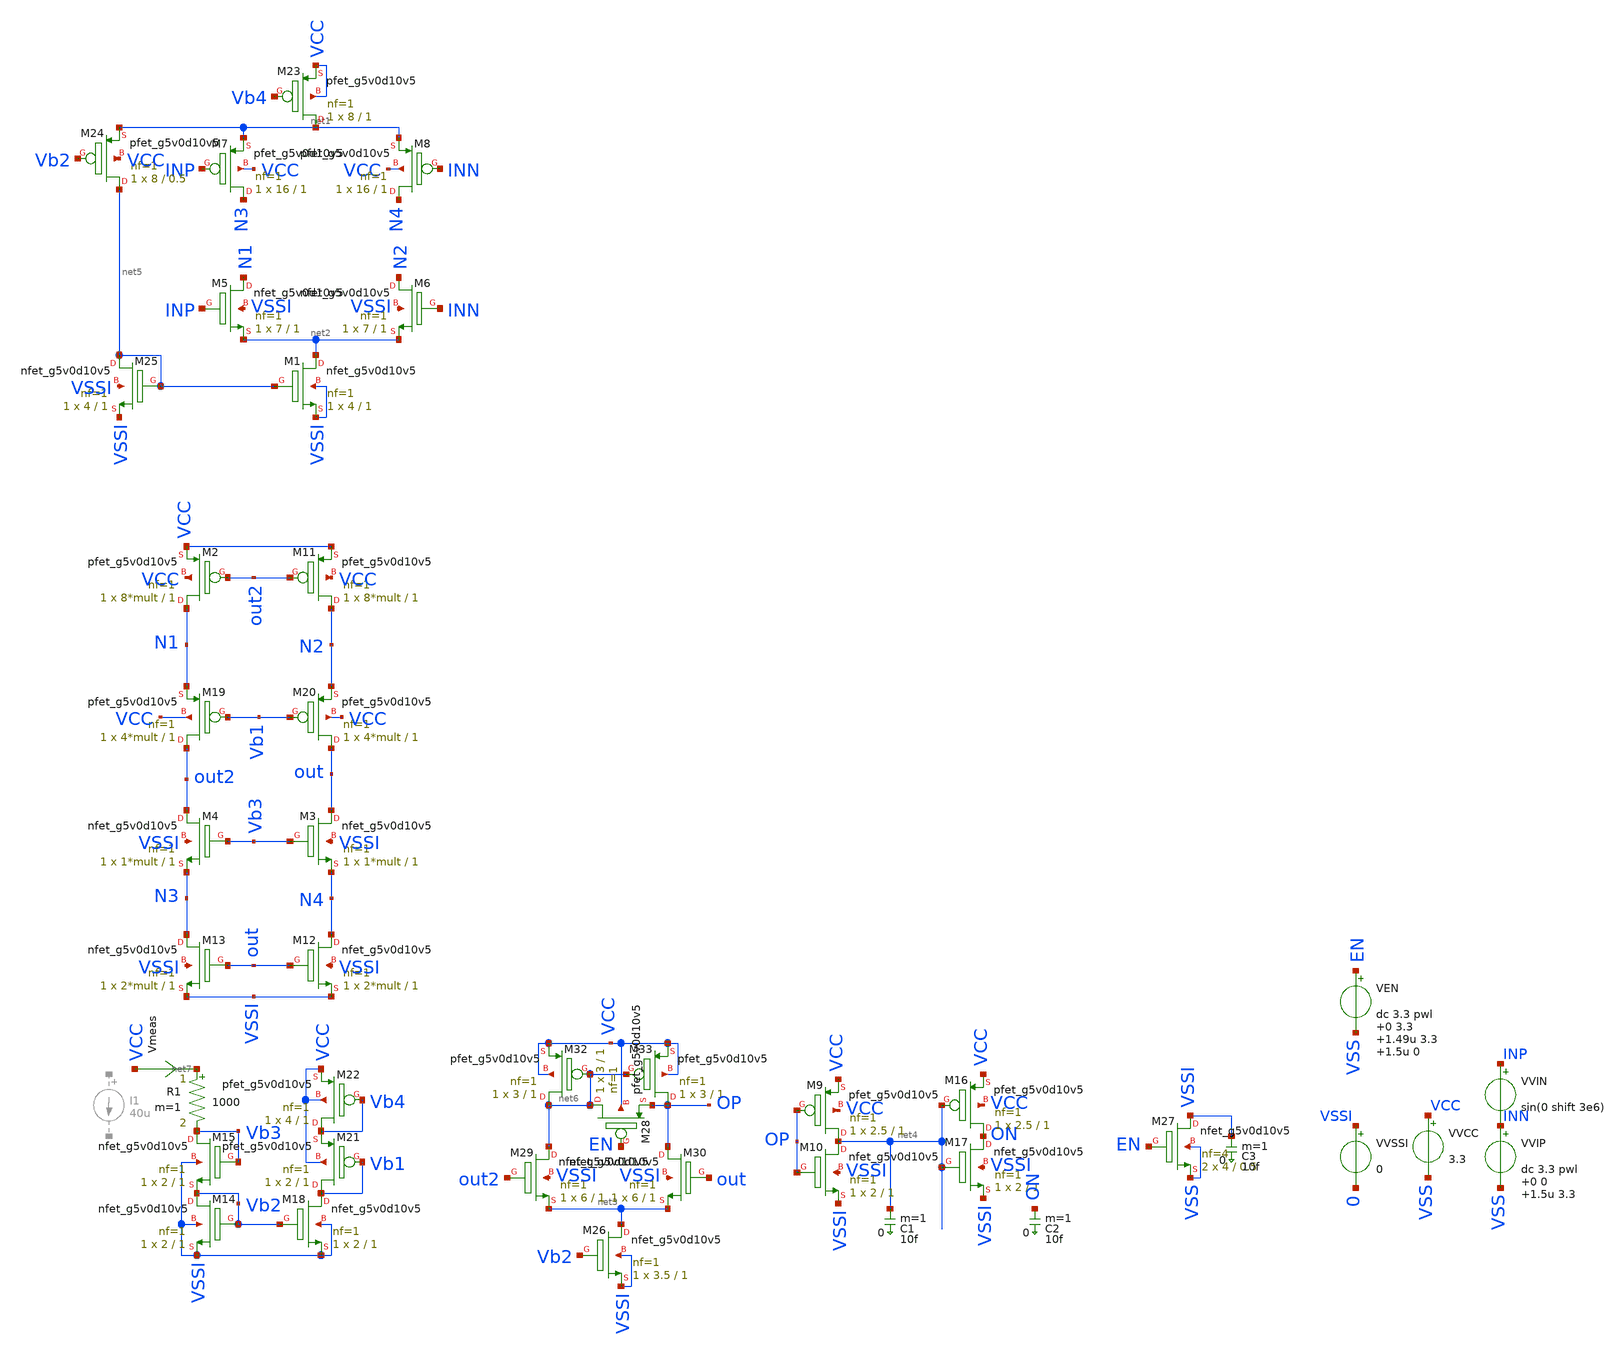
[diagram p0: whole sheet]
** sch_path: folded_cascode/folded_cascode.sch
.lib $::SKYWATER_MODELS/sky130.lib.spice.ss.red ss
.include $::SKYWATER_STDCELLS/sky130_fd_sc_hd.spice

**.subckt folded_cascode
VVIN INP INN sin(0 shift 3e6)
VVSSI VSSI 0 0
VVCC VCC VSS 3.3
XM19 out2 Vb1 N1 VCC sky130_fd_pr__pfet_g5v0d10v5 L=1 W=4*mult nf=1 ad='int((nf+1)/2) * W/nf * 0.29'
+ as='int((nf+2)/2) * W/nf * 0.29' pd='2*int((nf+1)/2) * (W/nf + 0.29)' ps='2*int((nf+2)/2) * (W/nf + 0.29)'
+ nrd='0.29 / W' nrs='0.29 / W' sa=0 sb=0 sd=0 mult=1 m=1
XM20 out Vb1 N2 VCC sky130_fd_pr__pfet_g5v0d10v5 L=1 W=4*mult nf=1 ad='int((nf+1)/2) * W/nf * 0.29' as='int((nf+2)/2) * W/nf * 0.29'
+ pd='2*int((nf+1)/2) * (W/nf + 0.29)' ps='2*int((nf+2)/2) * (W/nf + 0.29)' nrd='0.29 / W' nrs='0.29 / W'
+ sa=0 sb=0 sd=0 mult=1 m=1
XM3 out Vb3 N4 VSSI sky130_fd_pr__nfet_g5v0d10v5 L=1 W=1*mult nf=1 ad='int((nf+1)/2) * W/nf * 0.29' as='int((nf+2)/2) * W/nf * 0.29'
+ pd='2*int((nf+1)/2) * (W/nf + 0.29)' ps='2*int((nf+2)/2) * (W/nf + 0.29)' nrd='0.29 / W' nrs='0.29 / W'
+ sa=0 sb=0 sd=0 mult=1 m=1
XM4 out2 Vb3 N3 VSSI sky130_fd_pr__nfet_g5v0d10v5 L=1 W=1*mult nf=1 ad='int((nf+1)/2) * W/nf * 0.29'
+ as='int((nf+2)/2) * W/nf * 0.29' pd='2*int((nf+1)/2) * (W/nf + 0.29)' ps='2*int((nf+2)/2) * (W/nf + 0.29)'
+ nrd='0.29 / W' nrs='0.29 / W' sa=0 sb=0 sd=0 mult=1 m=1
VVIP INN VSS dc 3.3 pwl 0 0 1.5u 3.3

XM5 N1 INP net2 VSSI sky130_fd_pr__nfet_g5v0d10v5 L=1 W=7 nf=1 ad='int((nf+1)/2) * W/nf * 0.29' as='int((nf+2)/2) * W/nf * 0.29'
+ pd='2*int((nf+1)/2) * (W/nf + 0.29)' ps='2*int((nf+2)/2) * (W/nf + 0.29)' nrd='0.29 / W' nrs='0.29 / W'
+ sa=0 sb=0 sd=0 mult=1 m=1
XM6 N2 INN net2 VSSI sky130_fd_pr__nfet_g5v0d10v5 L=1 W=7 nf=1 ad='int((nf+1)/2) * W/nf * 0.29' as='int((nf+2)/2) * W/nf * 0.29'
+ pd='2*int((nf+1)/2) * (W/nf + 0.29)' ps='2*int((nf+2)/2) * (W/nf + 0.29)' nrd='0.29 / W' nrs='0.29 / W'
+ sa=0 sb=0 sd=0 mult=1 m=1
XM7 N3 INP net1 VCC sky130_fd_pr__pfet_g5v0d10v5 L=1 W=16 nf=1 ad='int((nf+1)/2) * W/nf * 0.29' as='int((nf+2)/2) * W/nf * 0.29'
+ pd='2*int((nf+1)/2) * (W/nf + 0.29)' ps='2*int((nf+2)/2) * (W/nf + 0.29)' nrd='0.29 / W' nrs='0.29 / W'
+ sa=0 sb=0 sd=0 mult=1 m=1
XM8 N4 INN net1 VCC sky130_fd_pr__pfet_g5v0d10v5 L=1 W=16 nf=1 ad='int((nf+1)/2) * W/nf * 0.29' as='int((nf+2)/2) * W/nf * 0.29'
+ pd='2*int((nf+1)/2) * (W/nf + 0.29)' ps='2*int((nf+2)/2) * (W/nf + 0.29)' nrd='0.29 / W' nrs='0.29 / W'
+ sa=0 sb=0 sd=0 mult=1 m=1
XM1 net2 net5 VSSI VSSI sky130_fd_pr__nfet_g5v0d10v5 L=1 W=4 nf=1 ad='int((nf+1)/2) * W/nf * 0.29' as='int((nf+2)/2) * W/nf * 0.29'
+ pd='2*int((nf+1)/2) * (W/nf + 0.29)' ps='2*int((nf+2)/2) * (W/nf + 0.29)' nrd='0.29 / W' nrs='0.29 / W'
+ sa=0 sb=0 sd=0 mult=1 m=1
XM2 N1 out2 VCC VCC sky130_fd_pr__pfet_g5v0d10v5 L=1 W=8*mult nf=1 ad='int((nf+1)/2) * W/nf * 0.29' as='int((nf+2)/2) * W/nf * 0.29'
+ pd='2*int((nf+1)/2) * (W/nf + 0.29)' ps='2*int((nf+2)/2) * (W/nf + 0.29)' nrd='0.29 / W' nrs='0.29 / W'
+ sa=0 sb=0 sd=0 mult=1 m=1
XM11 N2 out2 VCC VCC sky130_fd_pr__pfet_g5v0d10v5 L=1 W=8*mult nf=1 ad='int((nf+1)/2) * W/nf * 0.29'
+ as='int((nf+2)/2) * W/nf * 0.29' pd='2*int((nf+1)/2) * (W/nf + 0.29)' ps='2*int((nf+2)/2) * (W/nf + 0.29)'
+ nrd='0.29 / W' nrs='0.29 / W' sa=0 sb=0 sd=0 mult=1 m=1
XM12 N4 out VSSI VSSI sky130_fd_pr__nfet_g5v0d10v5 L=1 W=2*mult nf=1 ad='int((nf+1)/2) * W/nf * 0.29'
+ as='int((nf+2)/2) * W/nf * 0.29' pd='2*int((nf+1)/2) * (W/nf + 0.29)' ps='2*int((nf+2)/2) * (W/nf + 0.29)'
+ nrd='0.29 / W' nrs='0.29 / W' sa=0 sb=0 sd=0 mult=1 m=1
XM13 N3 out VSSI VSSI sky130_fd_pr__nfet_g5v0d10v5 L=1 W=2*mult nf=1 ad='int((nf+1)/2) * W/nf * 0.29'
+ as='int((nf+2)/2) * W/nf * 0.29' pd='2*int((nf+1)/2) * (W/nf + 0.29)' ps='2*int((nf+2)/2) * (W/nf + 0.29)'
+ nrd='0.29 / W' nrs='0.29 / W' sa=0 sb=0 sd=0 mult=1 m=1
XM14 Vb2 Vb2 VSSI VSSI sky130_fd_pr__nfet_g5v0d10v5 L=1 W=2 nf=1 ad='int((nf+1)/2) * W/nf * 0.29' as='int((nf+2)/2) * W/nf * 0.29'
+ pd='2*int((nf+1)/2) * (W/nf + 0.29)' ps='2*int((nf+2)/2) * (W/nf + 0.29)' nrd='0.29 / W' nrs='0.29 / W'
+ sa=0 sb=0 sd=0 mult=1 m=1
XM15 Vb3 Vb3 Vb2 VSSI sky130_fd_pr__nfet_g5v0d10v5 L=1 W=2 nf=1 ad='int((nf+1)/2) * W/nf * 0.29' as='int((nf+2)/2) * W/nf * 0.29'
+ pd='2*int((nf+1)/2) * (W/nf + 0.29)' ps='2*int((nf+2)/2) * (W/nf + 0.29)' nrd='0.29 / W' nrs='0.29 / W'
+ sa=0 sb=0 sd=0 mult=1 m=1
XM18 Vb1 Vb2 VSSI VSSI sky130_fd_pr__nfet_g5v0d10v5 L=1 W=2 nf=1 ad='int((nf+1)/2) * W/nf * 0.29' as='int((nf+2)/2) * W/nf * 0.29'
+ pd='2*int((nf+1)/2) * (W/nf + 0.29)' ps='2*int((nf+2)/2) * (W/nf + 0.29)' nrd='0.29 / W' nrs='0.29 / W'
+ sa=0 sb=0 sd=0 mult=1 m=1
XM21 Vb1 Vb1 Vb4 VCC sky130_fd_pr__pfet_g5v0d10v5 L=1 W=2 nf=1 ad='int((nf+1)/2) * W/nf * 0.29' as='int((nf+2)/2) * W/nf * 0.29'
+ pd='2*int((nf+1)/2) * (W/nf + 0.29)' ps='2*int((nf+2)/2) * (W/nf + 0.29)' nrd='0.29 / W' nrs='0.29 / W'
+ sa=0 sb=0 sd=0 mult=1 m=1
XM22 Vb4 Vb4 VCC VCC sky130_fd_pr__pfet_g5v0d10v5 L=1 W=4 nf=1 ad='int((nf+1)/2) * W/nf * 0.29' as='int((nf+2)/2) * W/nf * 0.29'
+ pd='2*int((nf+1)/2) * (W/nf + 0.29)' ps='2*int((nf+2)/2) * (W/nf + 0.29)' nrd='0.29 / W' nrs='0.29 / W'
+ sa=0 sb=0 sd=0 mult=1 m=1
XM23 net1 Vb4 VCC VCC sky130_fd_pr__pfet_g5v0d10v5 L=1 W=8 nf=1 ad='int((nf+1)/2) * W/nf * 0.29' as='int((nf+2)/2) * W/nf * 0.29'
+ pd='2*int((nf+1)/2) * (W/nf + 0.29)' ps='2*int((nf+2)/2) * (W/nf + 0.29)' nrd='0.29 / W' nrs='0.29 / W'
+ sa=0 sb=0 sd=0 mult=1 m=1
XM29 net6 out2 net3 VSSI sky130_fd_pr__nfet_g5v0d10v5 L=1 W=6 nf=1 ad='int((nf+1)/2) * W/nf * 0.29' as='int((nf+2)/2) * W/nf * 0.29'
+ pd='2*int((nf+1)/2) * (W/nf + 0.29)' ps='2*int((nf+2)/2) * (W/nf + 0.29)' nrd='0.29 / W' nrs='0.29 / W'
+ sa=0 sb=0 sd=0 mult=1 m=1
XM30 OP out net3 VSSI sky130_fd_pr__nfet_g5v0d10v5 L=1 W=6 nf=1 ad='int((nf+1)/2) * W/nf * 0.29' as='int((nf+2)/2) * W/nf * 0.29'
+ pd='2*int((nf+1)/2) * (W/nf + 0.29)' ps='2*int((nf+2)/2) * (W/nf + 0.29)' nrd='0.29 / W' nrs='0.29 / W'
+ sa=0 sb=0 sd=0 mult=1 m=1
XM32 net6 net6 VCC VCC sky130_fd_pr__pfet_g5v0d10v5 L=1 W=3 nf=1 ad='int((nf+1)/2) * W/nf * 0.29' as='int((nf+2)/2) * W/nf * 0.29'
+ pd='2*int((nf+1)/2) * (W/nf + 0.29)' ps='2*int((nf+2)/2) * (W/nf + 0.29)' nrd='0.29 / W' nrs='0.29 / W'
+ sa=0 sb=0 sd=0 mult=1 m=1
XM33 OP net6 VCC VCC sky130_fd_pr__pfet_g5v0d10v5 L=1 W=3 nf=1 ad='int((nf+1)/2) * W/nf * 0.29' as='int((nf+2)/2) * W/nf * 0.29'
+ pd='2*int((nf+1)/2) * (W/nf + 0.29)' ps='2*int((nf+2)/2) * (W/nf + 0.29)' nrd='0.29 / W' nrs='0.29 / W'
+ sa=0 sb=0 sd=0 mult=1 m=1
XM9 net4 OP VCC VCC sky130_fd_pr__pfet_g5v0d10v5 L=1 W=2.5 nf=1 ad='int((nf+1)/2) * W/nf * 0.29' as='int((nf+2)/2) * W/nf * 0.29'
+ pd='2*int((nf+1)/2) * (W/nf + 0.29)' ps='2*int((nf+2)/2) * (W/nf + 0.29)' nrd='0.29 / W' nrs='0.29 / W'
+ sa=0 sb=0 sd=0 mult=1 m=1
XM10 net4 OP VSSI VSSI sky130_fd_pr__nfet_g5v0d10v5 L=1 W=2 nf=1 ad='int((nf+1)/2) * W/nf * 0.29' as='int((nf+2)/2) * W/nf * 0.29'
+ pd='2*int((nf+1)/2) * (W/nf + 0.29)' ps='2*int((nf+2)/2) * (W/nf + 0.29)' nrd='0.29 / W' nrs='0.29 / W'
+ sa=0 sb=0 sd=0 mult=1 m=1
XM16 ON net4 VCC VCC sky130_fd_pr__pfet_g5v0d10v5 L=1 W=2.5 nf=1 ad='int((nf+1)/2) * W/nf * 0.29' as='int((nf+2)/2) * W/nf * 0.29'
+ pd='2*int((nf+1)/2) * (W/nf + 0.29)' ps='2*int((nf+2)/2) * (W/nf + 0.29)' nrd='0.29 / W' nrs='0.29 / W'
+ sa=0 sb=0 sd=0 mult=1 m=1
XM17 ON net4 VSSI VSSI sky130_fd_pr__nfet_g5v0d10v5 L=1 W=2 nf=1 ad='int((nf+1)/2) * W/nf * 0.29' as='int((nf+2)/2) * W/nf * 0.29'
+ pd='2*int((nf+1)/2) * (W/nf + 0.29)' ps='2*int((nf+2)/2) * (W/nf + 0.29)' nrd='0.29 / W' nrs='0.29 / W'
+ sa=0 sb=0 sd=0 mult=1 m=1
C1 net4 0 10f m=1
C2 ON 0 10f m=1
XM24 net5 Vb2 net1 VCC sky130_fd_pr__pfet_g5v0d10v5 L=0.5 W=8 nf=1 ad='int((nf+1)/2) * W/nf * 0.29' as='int((nf+2)/2) * W/nf * 0.29'
+ pd='2*int((nf+1)/2) * (W/nf + 0.29)' ps='2*int((nf+2)/2) * (W/nf + 0.29)' nrd='0.29 / W' nrs='0.29 / W'
+ sa=0 sb=0 sd=0 mult=1 m=1
XM25 net5 net5 VSSI VSSI sky130_fd_pr__nfet_g5v0d10v5 L=1 W=4 nf=1 ad='int((nf+1)/2) * W/nf * 0.29' as='int((nf+2)/2) * W/nf * 0.29'
+ pd='2*int((nf+1)/2) * (W/nf + 0.29)' ps='2*int((nf+2)/2) * (W/nf + 0.29)' nrd='0.29 / W' nrs='0.29 / W'
+ sa=0 sb=0 sd=0 mult=1 m=1
XM26 net3 Vb2 VSSI VSSI sky130_fd_pr__nfet_g5v0d10v5 L=1 W=3.5 nf=1 ad='int((nf+1)/2) * W/nf * 0.29'
+ as='int((nf+2)/2) * W/nf * 0.29' pd='2*int((nf+1)/2) * (W/nf + 0.29)' ps='2*int((nf+2)/2) * (W/nf + 0.29)'
+ nrd='0.29 / W' nrs='0.29 / W' sa=0 sb=0 sd=0 mult=1 m=1
XM27 VSSI EN VSS VSS sky130_fd_pr__nfet_g5v0d10v5 L=0.5 W=4 nf=4 ad='int((nf+1)/2) * W/nf * 0.29' as='int((nf+2)/2) * W/nf * 0.29'
+ pd='2*int((nf+1)/2) * (W/nf + 0.29)' ps='2*int((nf+2)/2) * (W/nf + 0.29)' nrd='0.29 / W' nrs='0.29 / W'
+ sa=0 sb=0 sd=0 mult=2 m=2
C3 VSSI 0 10f m=1
VEN EN VSS dc 3.3 pwl 0 3.3 1.49u 3.3 1.5u 0

XM28 net6 EN OP VCC sky130_fd_pr__pfet_g5v0d10v5 L=1 W=3 nf=1 ad='int((nf+1)/2) * W/nf * 0.29' as='int((nf+2)/2) * W/nf * 0.29'
+ pd='2*int((nf+1)/2) * (W/nf + 0.29)' ps='2*int((nf+2)/2) * (W/nf + 0.29)' nrd='0.29 / W' nrs='0.29 / W'
+ sa=0 sb=0 sd=0 mult=1 m=1
R1 net7 Vb3 1000 m=1
Vmeas VCC net7 0
.save i(vmeas)
**** begin user architecture code


.param mult = 5
.param shift = 1m
.option savecurrents
.save all
.save @m.xm8.msky130_fd_pr__pfet_g5v0d10v5[gm]
.save @m.xm6.msky130_fd_pr__nfet_g5v0d10v5[gm]
.tran 5n 2u
*.dc VVIP 0 3.3 0.1

**** interactive sim
.control
set color0=white
run
*set filetype=ascii
write folded_cascode.raw
quit
.endc


**** end user architecture code
**.ends
.end
